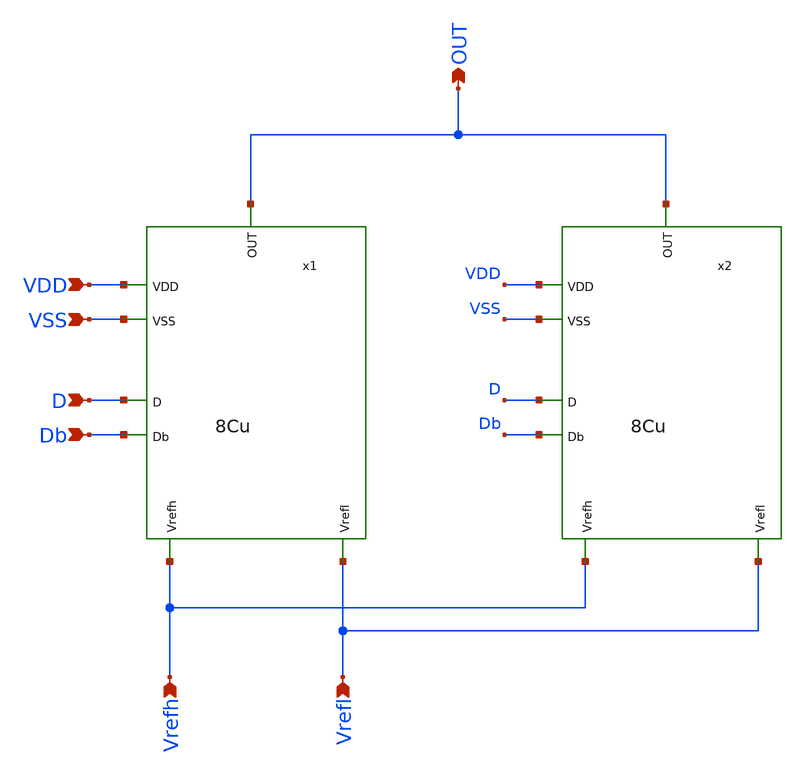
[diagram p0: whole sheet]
** sch_path: 16Cu.sch
**.subckt 16Cu OUT VDD D VSS Vrefh Vrefl Db
*.opin OUT
*.ipin VDD
*.ipin D
*.ipin VSS
*.ipin Vrefh
*.ipin Vrefl
*.ipin Db
x1 OUT VSS VDD Db D Vrefl Vrefh 8Cu
x2 OUT VSS VDD Db D Vrefl Vrefh 8Cu
**.ends
.end
